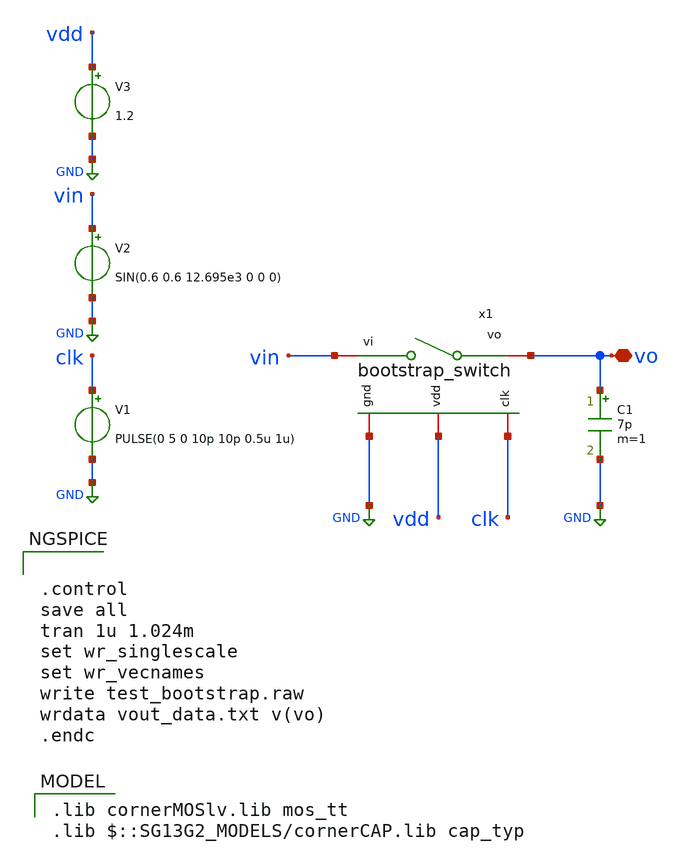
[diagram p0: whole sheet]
** sch_path: dependencies/ADC/dependencies/SAR_ADC_8BIT_IHP/xschem/bootstrap_switch_tbs.sch
**.subckt bootstrap_switch_tbs vo
*.iopin vo
V1 clk GND PULSE(0 5 0 10p 10p 0.5u 1u)
V2 vin GND SIN(0.6 0.6 12.695e3 0 0 0)
V3 vdd GND 1.2
C1 vo GND 7p m=1
x1 vdd vin vo clk GND bootstrap_switch
**** begin user architecture code
 .lib cornerMOSlv.lib mos_tt
.lib $::SG13G2_MODELS/cornerCAP.lib cap_typ



.control
save all
tran 1u 1.024m
set wr_singlescale
set wr_vecnames
write test_bootstrap.raw
wrdata vout_data.txt v(vo)
.endc


**** end user architecture code
**.ends
.GLOBAL GND
.end
